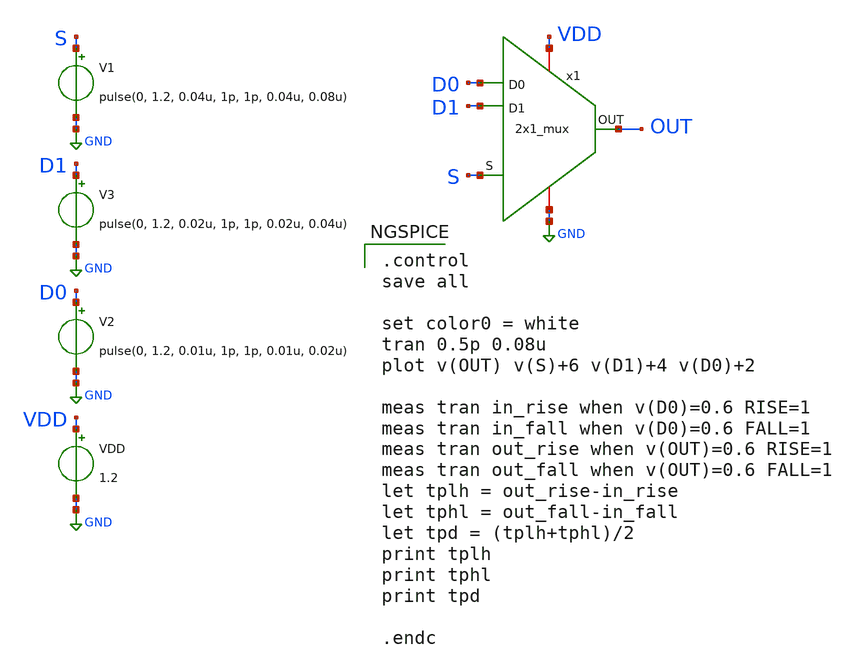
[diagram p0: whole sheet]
** sch_path: design/2x1_MUX/xschem/2x1_mux_tb.sch
**.subckt 2x1_mux_tb
V1 S GND pulse(0, 1.2, 0.04u, 1p, 1p, 0.04u, 0.08u)
V2 D0 GND pulse(0, 1.2, 0.01u, 1p, 1p, 0.01u, 0.02u)
V3 D1 GND pulse(0, 1.2, 0.02u, 1p, 1p, 0.02u, 0.04u)
VDD VDD GND 1.2
x1 GND VDD S D0 D1 OUT 2x1_mux
**** begin user architecture code

** opencircuitdesign pdks install
.lib $::SKYWATER_MODELS/sky130.lib.spice tt_mm



.control
save all

set color0 = white
tran 0.5p 0.08u
plot v(OUT) v(S)+6 v(D1)+4 v(D0)+2

meas tran in_rise when v(D0)=0.6 RISE=1
meas tran in_fall when v(D0)=0.6 FALL=1
meas tran out_rise when v(OUT)=0.6 RISE=1
meas tran out_fall when v(OUT)=0.6 FALL=1
let tplh = out_rise-in_rise
let tphl = out_fall-in_fall
let tpd = (tplh+tphl)/2
print tplh
print tphl
print tpd

.endc

**** end user architecture code
**.ends
.GLOBAL GND
.end
